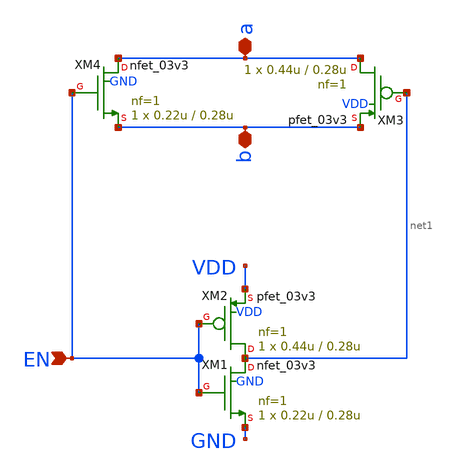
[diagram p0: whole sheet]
** sch_path: xschem_designs/transm_gate.sch
**.subckt transm_gate b a EN
*.iopin b
*.iopin a
*.ipin EN
XM1 net1 EN GND GND nfet_03v3 L=0.28u W=0.22u nf=1 ad='int((nf+1)/2) * W/nf * 0.18u' as='int((nf+2)/2) * W/nf * 0.18u'
+ pd='2*int((nf+1)/2) * (W/nf + 0.18u)' ps='2*int((nf+2)/2) * (W/nf + 0.18u)' nrd='0.18u / W' nrs='0.18u / W'
+ sa=0 sb=0 sd=0 m=1 par=1
XM2 net1 EN VDD VDD pfet_03v3 L=0.28u W=0.44u nf=1 ad='int((nf+1)/2) * W/nf * 0.18u' as='int((nf+2)/2) * W/nf * 0.18u'
+ pd='2*int((nf+1)/2) * (W/nf + 0.18u)' ps='2*int((nf+2)/2) * (W/nf + 0.18u)' nrd='0.18u / W' nrs='0.18u / W'
+ sa=0 sb=0 sd=0 m=1 par=1
XM3 a net1 b VDD pfet_03v3 L=0.28u W=0.44u nf=1 ad='int((nf+1)/2) * W/nf * 0.18u' as='int((nf+2)/2) * W/nf * 0.18u'
+ pd='2*int((nf+1)/2) * (W/nf + 0.18u)' ps='2*int((nf+2)/2) * (W/nf + 0.18u)' nrd='0.18u / W' nrs='0.18u / W'
+ sa=0 sb=0 sd=0 m=1 par=1
XM4 a EN b GND nfet_03v3 L=0.28u W=0.22u nf=1 ad='int((nf+1)/2) * W/nf * 0.18u' as='int((nf+2)/2) * W/nf * 0.18u'
+ pd='2*int((nf+1)/2) * (W/nf + 0.18u)' ps='2*int((nf+2)/2) * (W/nf + 0.18u)' nrd='0.18u / W' nrs='0.18u / W'
+ sa=0 sb=0 sd=0 m=1 par=1
**.ends
.end
